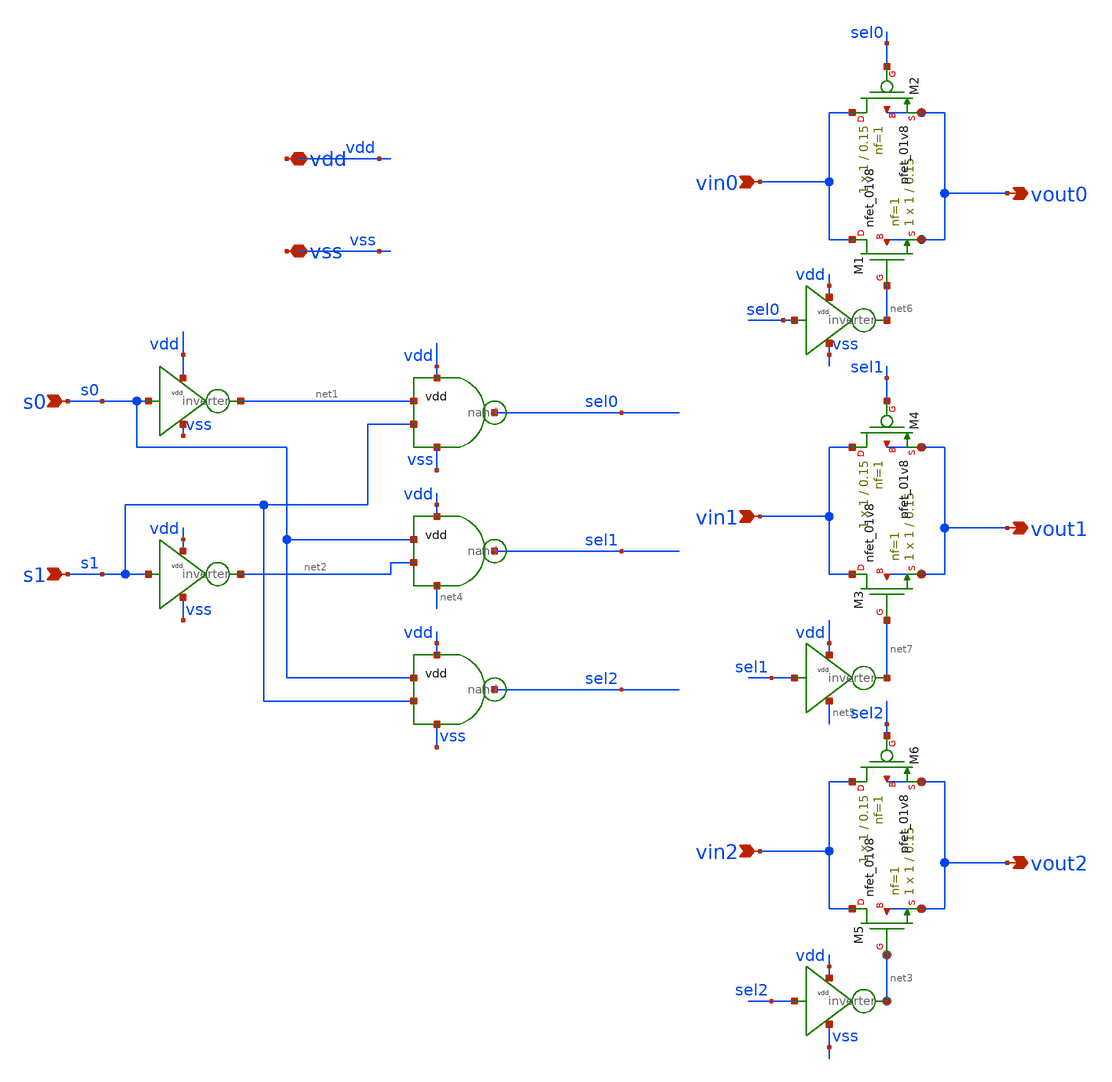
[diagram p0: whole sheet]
** sch_path: xschem/src/output_select/out_select.sch
**.subckt out_select vin0 vout0 vin1 vout1 vin2 vout2 vdd vss s0 s1
*.ipin vin0
*.opin vout0
*.ipin vin1
*.opin vout1
*.ipin vin2
*.opin vout2
*.iopin vdd
*.iopin vss
*.ipin s0
*.ipin s1
x4 vdd sel0 net1 s1 vss nand
x5 vdd sel1 s0 net2 net4 nand
x6 vdd sel2 s0 s1 vss nand
x8 vdd s1 net2 vss inverter
x9 vdd s0 net1 vss inverter
x7 vdd sel2 net3 vss inverter
x10 vdd sel1 net7 net5 inverter
x11 vdd sel0 net6 vss inverter
XM1 vin0 net6 vout0 vout0 sky130_fd_pr__nfet_01v8 L=0.15 W=1 nf=1 ad='int((nf+1)/2) * W/nf * 0.29' as='int((nf+2)/2) * W/nf * 0.29'
+ pd='2*int((nf+1)/2) * (W/nf + 0.29)' ps='2*int((nf+2)/2) * (W/nf + 0.29)' nrd='0.29 / W' nrs='0.29 / W'
+ sa=0 sb=0 sd=0 mult=1 m=1
XM2 vin0 sel0 vout0 vout0 sky130_fd_pr__pfet_01v8 L=0.15 W=1 nf=1 ad='int((nf+1)/2) * W/nf * 0.29' as='int((nf+2)/2) * W/nf * 0.29'
+ pd='2*int((nf+1)/2) * (W/nf + 0.29)' ps='2*int((nf+2)/2) * (W/nf + 0.29)' nrd='0.29 / W' nrs='0.29 / W'
+ sa=0 sb=0 sd=0 mult=1 m=1
XM3 vin1 net7 vout1 vout1 sky130_fd_pr__nfet_01v8 L=0.15 W=1 nf=1 ad='int((nf+1)/2) * W/nf * 0.29' as='int((nf+2)/2) * W/nf * 0.29'
+ pd='2*int((nf+1)/2) * (W/nf + 0.29)' ps='2*int((nf+2)/2) * (W/nf + 0.29)' nrd='0.29 / W' nrs='0.29 / W'
+ sa=0 sb=0 sd=0 mult=1 m=1
XM4 vin1 sel1 vout1 vout1 sky130_fd_pr__pfet_01v8 L=0.15 W=1 nf=1 ad='int((nf+1)/2) * W/nf * 0.29' as='int((nf+2)/2) * W/nf * 0.29'
+ pd='2*int((nf+1)/2) * (W/nf + 0.29)' ps='2*int((nf+2)/2) * (W/nf + 0.29)' nrd='0.29 / W' nrs='0.29 / W'
+ sa=0 sb=0 sd=0 mult=1 m=1
XM5 vin2 net3 vout2 vout2 sky130_fd_pr__nfet_01v8 L=0.15 W=1 nf=1 ad='int((nf+1)/2) * W/nf * 0.29' as='int((nf+2)/2) * W/nf * 0.29'
+ pd='2*int((nf+1)/2) * (W/nf + 0.29)' ps='2*int((nf+2)/2) * (W/nf + 0.29)' nrd='0.29 / W' nrs='0.29 / W'
+ sa=0 sb=0 sd=0 mult=1 m=1
XM6 vin2 sel2 vout2 vout2 sky130_fd_pr__pfet_01v8 L=0.15 W=1 nf=1 ad='int((nf+1)/2) * W/nf * 0.29' as='int((nf+2)/2) * W/nf * 0.29'
+ pd='2*int((nf+1)/2) * (W/nf + 0.29)' ps='2*int((nf+2)/2) * (W/nf + 0.29)' nrd='0.29 / W' nrs='0.29 / W'
+ sa=0 sb=0 sd=0 mult=1 m=1
**.ends

* expanding   symbol:  src/nand/nand.sym # of pins=5
** sym_path: xschem/src/nand/nand.sym
** sch_path: xschem/src/nand/nand.sch
.subckt nand vdd out A B vss
*.ipin A
*.ipin B
*.opin out
*.iopin vdd
*.iopin vss
XM1 out A net1 vss sky130_fd_pr__nfet_01v8 L=0.15 W=2 nf=1 ad='int((nf+1)/2) * W/nf * 0.29' as='int((nf+2)/2) * W/nf * 0.29'
+ pd='2*int((nf+1)/2) * (W/nf + 0.29)' ps='2*int((nf+2)/2) * (W/nf + 0.29)' nrd='0.29 / W' nrs='0.29 / W'
+ sa=0 sb=0 sd=0 mult=1 m=1
XM2 out A vdd vdd sky130_fd_pr__pfet_01v8 L=0.15 W=2 nf=1 ad='int((nf+1)/2) * W/nf * 0.29' as='int((nf+2)/2) * W/nf * 0.29'
+ pd='2*int((nf+1)/2) * (W/nf + 0.29)' ps='2*int((nf+2)/2) * (W/nf + 0.29)' nrd='0.29 / W' nrs='0.29 / W'
+ sa=0 sb=0 sd=0 mult=1 m=1
XM3 net1 B vss vss sky130_fd_pr__nfet_01v8 L=0.15 W=2 nf=1 ad='int((nf+1)/2) * W/nf * 0.29' as='int((nf+2)/2) * W/nf * 0.29'
+ pd='2*int((nf+1)/2) * (W/nf + 0.29)' ps='2*int((nf+2)/2) * (W/nf + 0.29)' nrd='0.29 / W' nrs='0.29 / W'
+ sa=0 sb=0 sd=0 mult=1 m=1
XM4 out B vdd vdd sky130_fd_pr__pfet_01v8 L=0.15 W=2 nf=1 ad='int((nf+1)/2) * W/nf * 0.29' as='int((nf+2)/2) * W/nf * 0.29'
+ pd='2*int((nf+1)/2) * (W/nf + 0.29)' ps='2*int((nf+2)/2) * (W/nf + 0.29)' nrd='0.29 / W' nrs='0.29 / W'
+ sa=0 sb=0 sd=0 mult=1 m=1
.ends


* expanding   symbol:  src/inverter/inverter.sym # of pins=4
** sym_path: xschem/src/inverter/inverter.sym
** sch_path: xschem/src/inverter/inverter.sch
.subckt inverter vdd A B vss
*.iopin vdd
*.iopin vss
*.ipin A
*.opin B
XM3 B A vss vss sky130_fd_pr__nfet_01v8 L=0.15 W=1 nf=1 ad='int((nf+1)/2) * W/nf * 0.29' as='int((nf+2)/2) * W/nf * 0.29'
+ pd='2*int((nf+1)/2) * (W/nf + 0.29)' ps='2*int((nf+2)/2) * (W/nf + 0.29)' nrd='0.29 / W' nrs='0.29 / W'
+ sa=0 sb=0 sd=0 mult=1 m=1
XM1 B A vdd vdd sky130_fd_pr__pfet_01v8 L=0.15 W=2 nf=1 ad='int((nf+1)/2) * W/nf * 0.29' as='int((nf+2)/2) * W/nf * 0.29'
+ pd='2*int((nf+1)/2) * (W/nf + 0.29)' ps='2*int((nf+2)/2) * (W/nf + 0.29)' nrd='0.29 / W' nrs='0.29 / W'
+ sa=0 sb=0 sd=0 mult=1 m=1
.ends

.end
